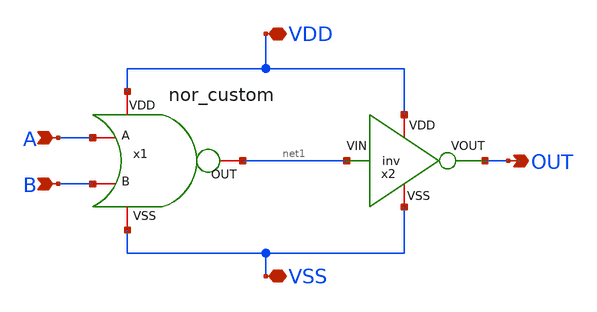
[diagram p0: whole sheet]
** sch_path: Custom_std_cells/or_custom.sch
**.subckt or_custom VDD VSS OUT A B
*.iopin VDD
*.iopin VSS
*.opin OUT
*.ipin A
*.ipin B
x1 VDD A net1 B VSS nor_custom
x2 VDD OUT net1 VSS inv
**.ends

* expanding   symbol:  /home/designer/shared/PhaseInterpolator/Custom_std_cells/nor_custom.sym # of
*+ pins=5
** sym_path: /home/designer/shared/PhaseInterpolator/Custom_std_cells/nor_custom.sym
** sch_path: /home/designer/shared/PhaseInterpolator/Custom_std_cells/nor_custom.sch
.subckt nor_custom VDD A OUT B VSS
*.iopin VDD
*.iopin VSS
*.ipin A
*.ipin B
*.opin OUT
XM1 OUT B VSS VSS sg13_lv_nmos w=0.15u l=0.13u ng=1 m=1 mm_ok=1
XM2 OUT B net1 VDD sg13_lv_pmos w=0.45u l=0.13u ng=1 m=1 mm_ok=1
XM3 OUT A VSS VSS sg13_lv_nmos w=0.15u l=0.13u ng=1 m=1 mm_ok=1
XM4 net1 A VDD VDD sg13_lv_pmos w=0.45u l=0.13u ng=1 m=1 mm_ok=1
.ends

.end
